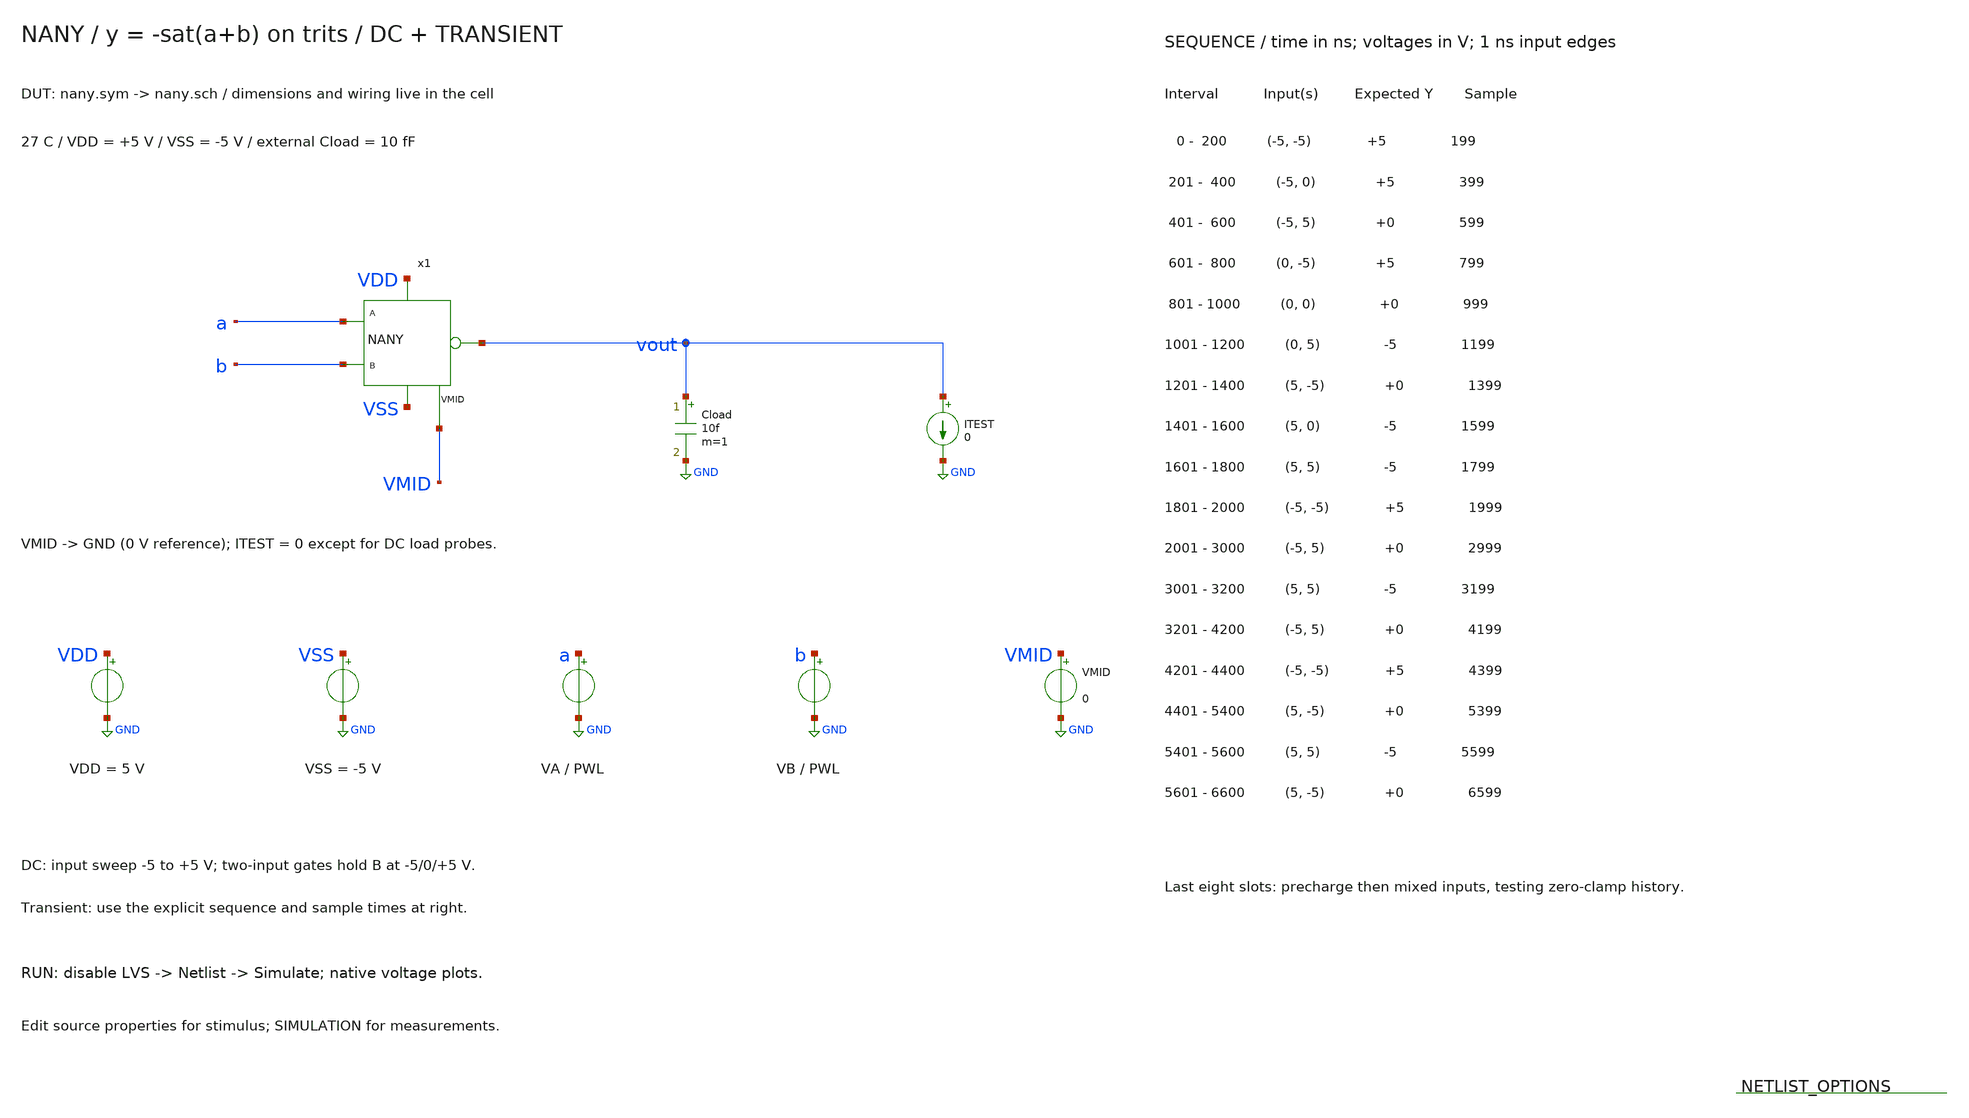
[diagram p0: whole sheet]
** sch_path: member_project/balanced-ternary-logic/PenguinEino/nany_tb.sch
**.subckt nany_tb
x1 a b vout VDD VSS VMID nany
Cload vout GND 10f m=1
ITEST vout GND 0
VDD VDD GND 5
VSS VSS GND -5
VA a GND PWL(0 -5 200n -5 201n -5 400n -5 401n -5 600n -5 601n 0 800n 0 801n 0 1000n 0 1001n 0 1200n
+ 0 1201n 5 1400n 5 1401n 5 1600n 5 1601n 5 1800n 5 1801n -5 2000n -5 2001n -5 3000n -5 3001n 5 3200n 5
+ 3201n -5 4200n -5 4201n -5 4400n -5 4401n 5 5400n 5 5401n 5 5600n 5 5601n 5 6600n 5)
VB b GND PWL(0 -5 200n -5 201n 0 400n 0 401n 5 600n 5 601n -5 800n -5 801n 0 1000n 0 1001n 5 1200n 5
+ 1201n -5 1400n -5 1401n 0 1600n 0 1601n 5 1800n 5 1801n -5 2000n -5 2001n 5 3000n 5 3001n 5 3200n 5 3201n
+ 5 4200n 5 4201n -5 4400n -5 4401n -5 5400n -5 5401n 5 5600n 5 5601n -5 6600n -5)
VMID VMID GND 0
**** begin user architecture code
 .include $::LIB/ip62_models

.temp 27
.options rshunt=1e12
.nodeset v(vout)=5 v(x1.net1)=5 v(x1.net2)=5 v(x1.net3)=-5 v(x1.net4)=-5 v(x1.net5)=0 v(x1.net6)=0
.control
save all
set wr_singlescale
set wr_vecnames
setplot const
let driven_failures=0
let mixed_failures=0
reset
alter VB -5
dc VA -5 5 0.015625
plot v(a) v(vout) ylimit -5.5 5.5 title 'NANY DC: B=-5 V'
wrdata nany_dc_b_neg.txt v(a) v(vout)
meas dc out_a_neg_b_neg find v(vout) at=-5
meas dc out_a_zero_b_neg find v(vout) at=0
meas dc out_a_pos_b_neg find v(vout) at=5
reset
alter VB 0
dc VA -5 5 0.015625
plot v(a) v(vout) ylimit -5.5 5.5 title 'NANY DC: B=0 V'
wrdata nany_dc_b_zero.txt v(a) v(vout)
meas dc out_a_neg_b_zero find v(vout) at=-5
meas dc out_a_zero_b_zero find v(vout) at=0
meas dc out_a_pos_b_zero find v(vout) at=5
reset
alter VB 5
dc VA -5 5 0.015625
plot v(a) v(vout) ylimit -5.5 5.5 title 'NANY DC: B=5 V'
wrdata nany_dc_b_pos.txt v(a) v(vout)
meas dc out_a_neg_b_pos find v(vout) at=-5
meas dc out_a_zero_b_pos find v(vout) at=0
meas dc out_a_pos_b_pos find v(vout) at=5
reset
echo ---- DC load sensitivity: +1nA draws current from output; -1nA injects ----
alter VA -5
alter VB -5
alter ITEST 0
op
let const.v_unloaded=v(vout)
alter ITEST 1n
op
let const.v_sink=v(vout)
alter ITEST -1n
op
let const.v_source=v(vout)
echo INPUT_A=-5 INPUT_B=-5
print const.v_unloaded const.v_sink const.v_source
let const.r_apparent=(const.v_source-const.v_sink)/2e-9
print const.r_apparent
alter VA -5
alter VB 0
alter ITEST 0
op
let const.v_unloaded=v(vout)
alter ITEST 1n
op
let const.v_sink=v(vout)
alter ITEST -1n
op
let const.v_source=v(vout)
echo INPUT_A=-5 INPUT_B=0
print const.v_unloaded const.v_sink const.v_source
let const.r_apparent=(const.v_source-const.v_sink)/2e-9
print const.r_apparent
alter VA -5
alter VB 5
alter ITEST 0
op
let const.v_unloaded=v(vout)
alter ITEST 1n
op
let const.v_sink=v(vout)
alter ITEST -1n
op
let const.v_source=v(vout)
echo INPUT_A=-5 INPUT_B=5
print const.v_unloaded const.v_sink const.v_source
let const.r_apparent=(const.v_source-const.v_sink)/2e-9
print const.r_apparent
alter VA 0
alter VB -5
alter ITEST 0
op
let const.v_unloaded=v(vout)
alter ITEST 1n
op
let const.v_sink=v(vout)
alter ITEST -1n
op
let const.v_source=v(vout)
echo INPUT_A=0 INPUT_B=-5
print const.v_unloaded const.v_sink const.v_source
let const.r_apparent=(const.v_source-const.v_sink)/2e-9
print const.r_apparent
alter VA 0
alter VB 0
alter ITEST 0
op
let const.v_unloaded=v(vout)
alter ITEST 1n
op
let const.v_sink=v(vout)
alter ITEST -1n
op
let const.v_source=v(vout)
echo INPUT_A=0 INPUT_B=0
print const.v_unloaded const.v_sink const.v_source
let const.r_apparent=(const.v_source-const.v_sink)/2e-9
print const.r_apparent
alter VA 0
alter VB 5
alter ITEST 0
op
let const.v_unloaded=v(vout)
alter ITEST 1n
op
let const.v_sink=v(vout)
alter ITEST -1n
op
let const.v_source=v(vout)
echo INPUT_A=0 INPUT_B=5
print const.v_unloaded const.v_sink const.v_source
let const.r_apparent=(const.v_source-const.v_sink)/2e-9
print const.r_apparent
alter VA 5
alter VB -5
alter ITEST 0
op
let const.v_unloaded=v(vout)
alter ITEST 1n
op
let const.v_sink=v(vout)
alter ITEST -1n
op
let const.v_source=v(vout)
echo INPUT_A=5 INPUT_B=-5
print const.v_unloaded const.v_sink const.v_source
let const.r_apparent=(const.v_source-const.v_sink)/2e-9
print const.r_apparent
alter VA 5
alter VB 0
alter ITEST 0
op
let const.v_unloaded=v(vout)
alter ITEST 1n
op
let const.v_sink=v(vout)
alter ITEST -1n
op
let const.v_source=v(vout)
echo INPUT_A=5 INPUT_B=0
print const.v_unloaded const.v_sink const.v_source
let const.r_apparent=(const.v_source-const.v_sink)/2e-9
print const.r_apparent
alter VA 5
alter VB 5
alter ITEST 0
op
let const.v_unloaded=v(vout)
alter ITEST 1n
op
let const.v_sink=v(vout)
alter ITEST -1n
op
let const.v_source=v(vout)
echo INPUT_A=5 INPUT_B=5
print const.v_unloaded const.v_sink const.v_source
let const.r_apparent=(const.v_source-const.v_sink)/2e-9
print const.r_apparent
reset
tran 0.2n 6600n
plot v(a) v(b) v(vout) title 'NANY: nine input pairs and mixed-rail history'
plot v(a) v(b) v(vout) xlimit 1.8u 6.6u title 'NANY: same mixed inputs after opposite precharges'
wrdata nany_tran.txt v(a) v(b) v(vout)
meas tran out_01 find v(vout) at=199n
if abs(out_01-(5)) > 0.5
let const.driven_failures=const.driven_failures+1
echo OUTSIDE_0.5V: sample 1 A=-5 B=-5 ideal=5
end
meas tran out_02 find v(vout) at=399n
if abs(out_02-(5)) > 0.5
let const.driven_failures=const.driven_failures+1
echo OUTSIDE_0.5V: sample 2 A=-5 B=0 ideal=5
end
meas tran out_03 find v(vout) at=599n
if abs(out_03-(0)) > 0.5
let const.mixed_failures=const.mixed_failures+1
echo OUTSIDE_0.5V: sample 3 A=-5 B=5 ideal=0
end
meas tran out_04 find v(vout) at=799n
if abs(out_04-(5)) > 0.5
let const.driven_failures=const.driven_failures+1
echo OUTSIDE_0.5V: sample 4 A=0 B=-5 ideal=5
end
meas tran out_05 find v(vout) at=999n
if abs(out_05-(0)) > 0.5
let const.driven_failures=const.driven_failures+1
echo OUTSIDE_0.5V: sample 5 A=0 B=0 ideal=0
end
meas tran out_06 find v(vout) at=1199n
if abs(out_06-(-5)) > 0.5
let const.driven_failures=const.driven_failures+1
echo OUTSIDE_0.5V: sample 6 A=0 B=5 ideal=-5
end
meas tran out_07 find v(vout) at=1399n
if abs(out_07-(0)) > 0.5
let const.mixed_failures=const.mixed_failures+1
echo OUTSIDE_0.5V: sample 7 A=5 B=-5 ideal=0
end
meas tran out_08 find v(vout) at=1599n
if abs(out_08-(-5)) > 0.5
let const.driven_failures=const.driven_failures+1
echo OUTSIDE_0.5V: sample 8 A=5 B=0 ideal=-5
end
meas tran out_09 find v(vout) at=1799n
if abs(out_09-(-5)) > 0.5
let const.driven_failures=const.driven_failures+1
echo OUTSIDE_0.5V: sample 9 A=5 B=5 ideal=-5
end
meas tran out_10 find v(vout) at=1999n
if abs(out_10-(5)) > 0.5
let const.driven_failures=const.driven_failures+1
echo OUTSIDE_0.5V: sample 10 A=-5 B=-5 ideal=5
end
meas tran out_11 find v(vout) at=2999n
if abs(out_11-(0)) > 0.5
let const.mixed_failures=const.mixed_failures+1
echo OUTSIDE_0.5V: sample 11 A=-5 B=5 ideal=0
end
meas tran out_12 find v(vout) at=3199n
if abs(out_12-(-5)) > 0.5
let const.driven_failures=const.driven_failures+1
echo OUTSIDE_0.5V: sample 12 A=5 B=5 ideal=-5
end
meas tran out_13 find v(vout) at=4199n
if abs(out_13-(0)) > 0.5
let const.mixed_failures=const.mixed_failures+1
echo OUTSIDE_0.5V: sample 13 A=-5 B=5 ideal=0
end
meas tran out_14 find v(vout) at=4399n
if abs(out_14-(5)) > 0.5
let const.driven_failures=const.driven_failures+1
echo OUTSIDE_0.5V: sample 14 A=-5 B=-5 ideal=5
end
meas tran out_15 find v(vout) at=5399n
if abs(out_15-(0)) > 0.5
let const.mixed_failures=const.mixed_failures+1
echo OUTSIDE_0.5V: sample 15 A=5 B=-5 ideal=0
end
meas tran out_16 find v(vout) at=5599n
if abs(out_16-(-5)) > 0.5
let const.driven_failures=const.driven_failures+1
echo OUTSIDE_0.5V: sample 16 A=5 B=5 ideal=-5
end
meas tran out_17 find v(vout) at=6599n
if abs(out_17-(0)) > 0.5
let const.mixed_failures=const.mixed_failures+1
echo OUTSIDE_0.5V: sample 17 A=5 B=-5 ideal=0
end
echo ---- Error counts: driven states vs mixed-rail clamp ----
print const.driven_failures const.mixed_failures
.endc

**** end user architecture code
**.ends

* expanding   symbol:  /home/ishi-kai/balanced-ternary-logic/nany.sym # of pins=6
** sym_path: member_project/balanced-ternary-logic/PenguinEino/submission/nany.sym
** sch_path: member_project/balanced-ternary-logic/PenguinEino/submission/nany.sch
.subckt nany a b vout VDD VSS VMID
*.iopin VDD
*.ipin a
*.ipin b
*.opin vout
*.iopin VSS
*.iopin VMID
XXM3 net2 b net1 VDD PMOS w=34u l=1u nrd=0 nrs=0 m=1
XR2 net2 vout VDD F_RR w=2.8e-06 l=30e-06 R=1 tc1=0 tc2=0 m=1
XR1 vout net3 VDD F_RR w=2.8e-06 l=30e-06 R=1 tc1=0 tc2=0 m=1
XXM2 net3 a net4 VSS NMOS w=11u l=1u nrd=0 nrs=0 m=1
XXM1 net4 b VSS VSS NMOS w=11u l=1u nrd=0 nrs=0 m=1
XXM5 net1 a VDD VDD PMOS w=34u l=1u nrd=0 nrs=0 m=1
XXM6 net5 a vout VDD PMOS w=14u l=1u nrd=0 nrs=0 m=1
XXM7 net5 b VMID VSS NMOS w=8u l=1u nrd=0 nrs=0 m=1
XXM8 net6 b vout VDD PMOS w=14u l=1u nrd=0 nrs=0 m=1
XXM9 net6 a VMID VSS NMOS w=8u l=1u nrd=0 nrs=0 m=1
.ends

.GLOBAL GND
.end
